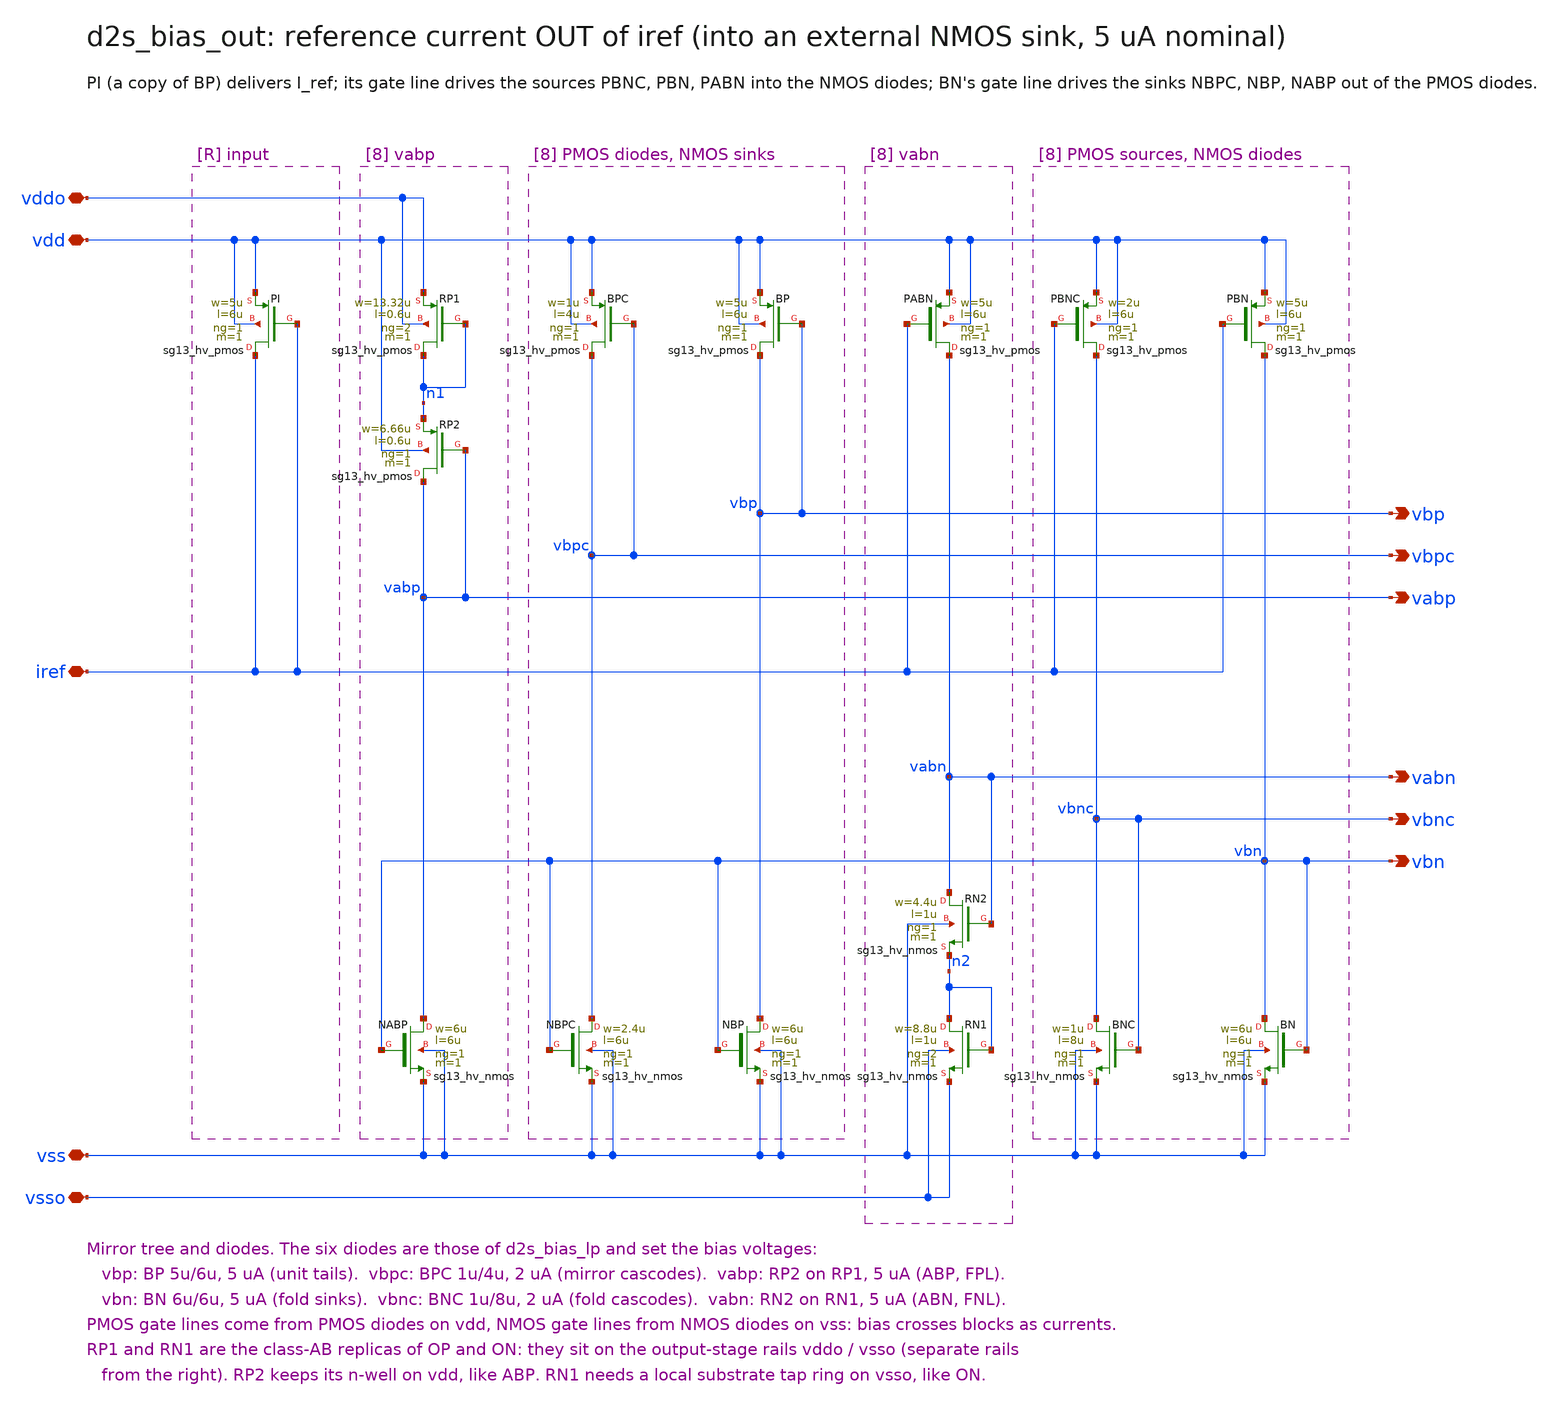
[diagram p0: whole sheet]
** sch_path: sudelbuecher/design_considerations/class_ab_pad_driver/improvements/xschem/d2s_bias_out.sch
**.subckt d2s_bias_out vdd vss vddo vsso iref vbp vbn vbpc vbnc vabp vabn
*.iopin vdd
*.iopin vss
*.iopin vddo
*.iopin vsso
*.iopin iref
*.opin vbp
*.opin vbn
*.opin vbpc
*.opin vbnc
*.opin vabp
*.opin vabn
XPI iref iref vdd vdd sg13_hv_pmos w=5u l=6u ng=1 m=1 mm_ok=1
XBPC vbpc vbpc vdd vdd sg13_hv_pmos w=1u l=4u ng=1 m=1 mm_ok=1
XNBPC vbpc vbn vss vss sg13_hv_nmos w=2.4u l=6u ng=1 m=1 mm_ok=1
XBP vbp vbp vdd vdd sg13_hv_pmos w=5u l=6u ng=1 m=1 mm_ok=1
XNBP vbp vbn vss vss sg13_hv_nmos w=6u l=6u ng=1 m=1 mm_ok=1
XRP1 n1 n1 vddo vddo sg13_hv_pmos w=13.32u l=0.6u ng=2 m=1 mm_ok=1
XRP2 vabp vabp n1 vdd sg13_hv_pmos w=6.66u l=0.6u ng=1 m=1 mm_ok=1
XNABP vabp vbn vss vss sg13_hv_nmos w=6u l=6u ng=1 m=1 mm_ok=1
XPBNC vbnc iref vdd vdd sg13_hv_pmos w=2u l=6u ng=1 m=1 mm_ok=1
XBNC vbnc vbnc vss vss sg13_hv_nmos w=1u l=8u ng=1 m=1 mm_ok=1
XPBN vbn iref vdd vdd sg13_hv_pmos w=5u l=6u ng=1 m=1 mm_ok=1
XBN vbn vbn vss vss sg13_hv_nmos w=6u l=6u ng=1 m=1 mm_ok=1
XPABN vabn iref vdd vdd sg13_hv_pmos w=5u l=6u ng=1 m=1 mm_ok=1
XRN2 vabn vabn n2 vss sg13_hv_nmos w=4.4u l=1u ng=1 m=1 mm_ok=1
XRN1 n2 n2 vsso vsso sg13_hv_nmos w=8.8u l=1u ng=2 m=1 mm_ok=1
**.ends
.end
